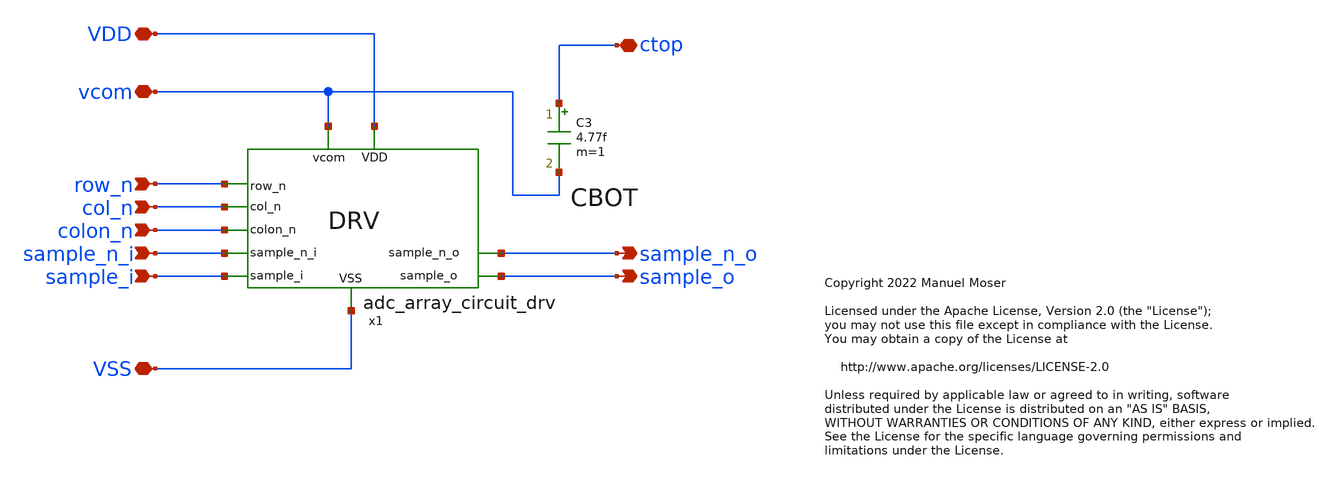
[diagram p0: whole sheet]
** sch_path: xschem/adc_array_wafflecap_8_drv.sch
* Copyright 2022 Manuel Moser
* Licensed under the Apache License, Version 2.0 (the "License");
**.subckt adc_array_wafflecap_8_drv sample_n_i sample_i vcom VDD ctop VSS sample_n_o sample_o row_n
*+ col_n colon_n
*.ipin sample_n_i
*.ipin sample_i
*.iopin vcom
*.iopin VDD
*.iopin ctop
*.iopin VSS
*.opin sample_n_o
*.opin sample_o
*.ipin row_n
*.ipin col_n
*.ipin colon_n
C3 ctop vcom 4.77f m=1
x1 VDD row_n col_n colon_n sample_n_i vcom sample_i VSS sample_n_o sample_o adc_array_circuit_drv
**.ends

* expanding   symbol:  adc_array_circuit_drv.sym # of pins=10
** sym_path: xschem/adc_array_circuit_drv.sym
** sch_path: xschem/adc_array_circuit_drv.sch
.subckt adc_array_circuit_drv VDD row_n col_n colon_n sample_n_i vcom sample_i VSS sample_n_o
+ sample_o
*.ipin sample_n_i
*.ipin sample_i
*.iopin vcom
*.ipin row_n
*.ipin col_n
*.ipin colon_n
*.iopin VDD
*.iopin VSS
*.opin sample_o
*.opin sample_n_o
XM6 VDD sample_n_i sample_o VDD sky130_fd_pr__pfet_01v8 L=0.15 W=1.6 nf=2 ad='int((nf+1)/2) * W/nf * 0.29'
+ as='int((nf+2)/2) * W/nf * 0.29' pd='2*int((nf+1)/2) * (W/nf + 0.29)' ps='2*int((nf+2)/2) * (W/nf + 0.29)'
+ nrd='0.29 / W' nrs='0.29 / W' sa=0 sb=0 sd=0 mult=1 m=1
XM7 VDD sample_i sample_n_o VDD sky130_fd_pr__pfet_01v8 L=0.15 W=1.6 nf=2 ad='int((nf+1)/2) * W/nf * 0.29'
+ as='int((nf+2)/2) * W/nf * 0.29' pd='2*int((nf+1)/2) * (W/nf + 0.29)' ps='2*int((nf+2)/2) * (W/nf + 0.29)'
+ nrd='0.29 / W' nrs='0.29 / W' sa=0 sb=0 sd=0 mult=1 m=1
XM9 VSS sample_i sample_n_o VSS sky130_fd_pr__nfet_01v8 L=0.15 W=0.84 nf=2 ad='int((nf+1)/2) * W/nf * 0.29'
+ as='int((nf+2)/2) * W/nf * 0.29' pd='2*int((nf+1)/2) * (W/nf + 0.29)' ps='2*int((nf+2)/2) * (W/nf + 0.29)'
+ nrd='0.29 / W' nrs='0.29 / W' sa=0 sb=0 sd=0 mult=1 m=1
XM10 VSS sample_n_i sample_o VSS sky130_fd_pr__nfet_01v8 L=0.15 W=0.84 nf=2 ad='int((nf+1)/2) * W/nf * 0.29'
+ as='int((nf+2)/2) * W/nf * 0.29' pd='2*int((nf+1)/2) * (W/nf + 0.29)' ps='2*int((nf+2)/2) * (W/nf + 0.29)'
+ nrd='0.29 / W' nrs='0.29 / W' sa=0 sb=0 sd=0 mult=1 m=1
* noconn row_n
* noconn col_n
* noconn colon_n
* noconn vcom
.ends

.end
